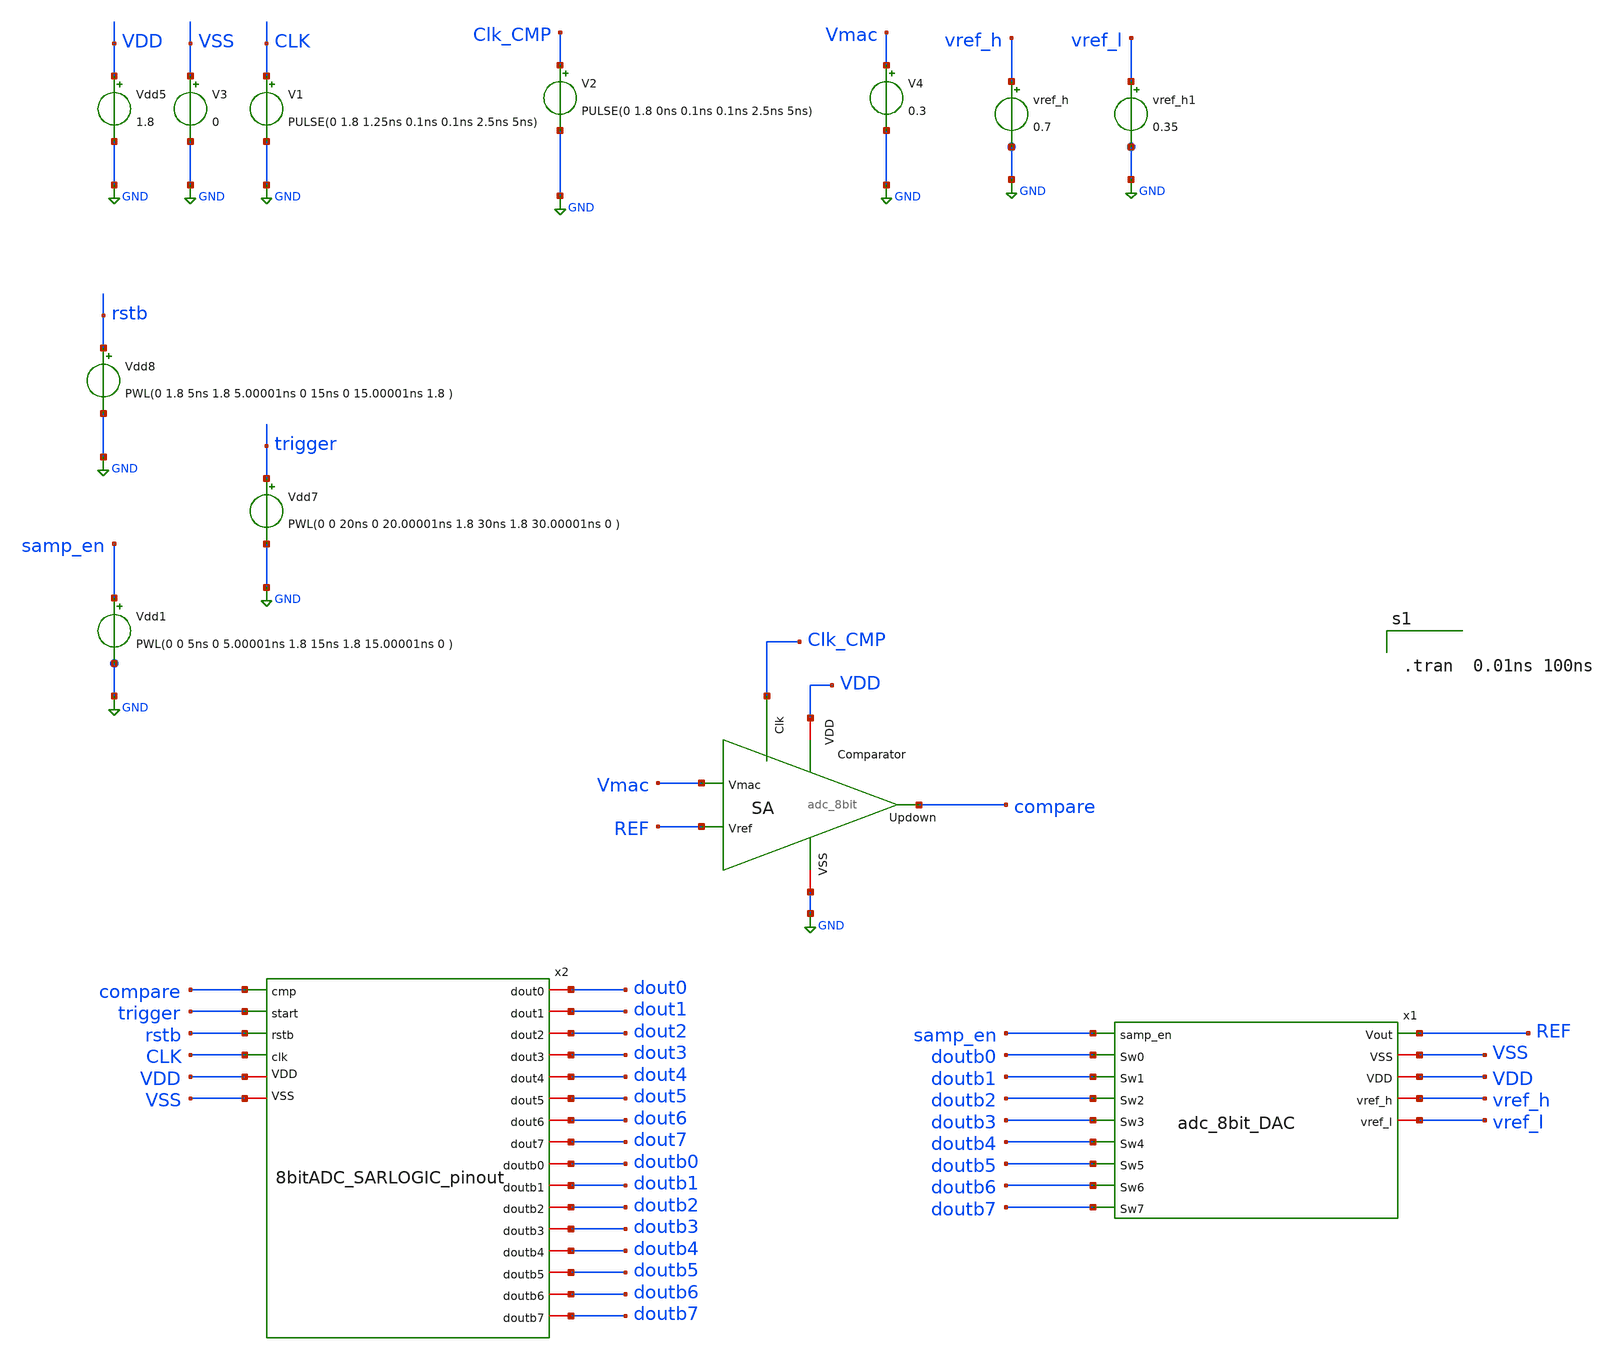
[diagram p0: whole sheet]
** sch_path: ADC_TB.sch
**.subckt ADC_TB
x1 REF VSS samp_en doutb0 VDD doutb1 vref_h doutb2 vref_l doutb3 doutb4 doutb5 doutb6 doutb7
+ adc_8bit_DAC
vref_h vref_h GND 0.7
Vdd5 VDD GND 1.8
V1 CLK GND PULSE(0 1.8 1.25ns 0.1ns 0.1ns 2.5ns 5ns)
V3 VSS GND 0
Vdd7 trigger GND PWL(0 0 20ns 0 20.00001ns 1.8 30ns 1.8 30.00001ns 0 )
Vdd8 rstb GND PWL(0 1.8 5ns 1.8 5.00001ns 0 15ns 0 15.00001ns 1.8 )
x2 VDD compare VSS trigger doutb0 dout0 rstb CLK doutb1 dout1 doutb2 dout2 dout3 doutb3 dout4 doutb4
+ dout5 doutb5 dout6 doutb6 doutb7 dout7 8bitADC_SARLOGIC_pinout
x3 GND VDD REF Clk_CMP Vmac compare adc_8bit
V4 Vmac GND 0.3
V2 Clk_CMP GND PULSE(0 1.8 0ns 0.1ns 0.1ns 2.5ns 5ns)
Vdd1 samp_en GND PWL(0 0 5ns 0 5.00001ns 1.8 15ns 1.8 15.00001ns 0 )
vref_h1 vref_l GND 0.35
**** begin user architecture code

** opencircuitdesign pdks install
.lib $::SKYWATER_MODELS/sky130.lib.spice tt
.include $::SKYWATER_STDCELLS/sky130_fd_sc_hd.spice



.tran  0.01ns 100ns



**** end user architecture code
**.ends
.GLOBAL GND
.end
